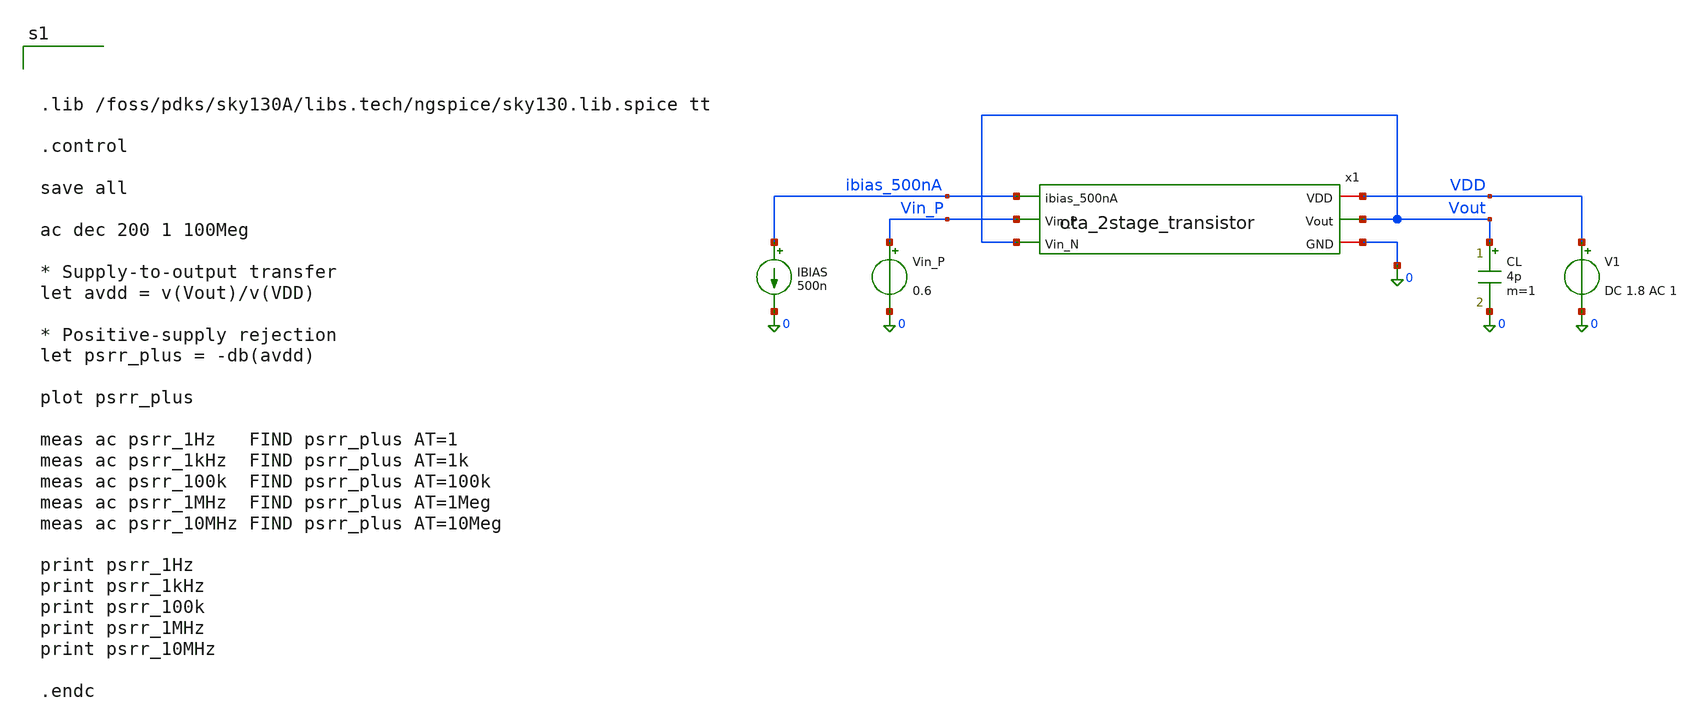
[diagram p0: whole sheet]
** sch_path: dfii/project_2stage_OTA_sim/tb_ota_2stage_psrr.sch
**.subckt tb_ota_2stage_psrr
x1 VDD ibias_500nA Vout Vin_P Vout 0 ota_2stage_transistor
V1 VDD 0 DC 1.8 AC 1
IBIAS ibias_500nA 0 500n
Vin_P Vin_P 0 0.6
CL Vout 0 4p m=1
**** begin user architecture code



.lib /foss/pdks/sky130A/libs.tech/ngspice/sky130.lib.spice tt

.control

save all

ac dec 200 1 100Meg

* Supply-to-output transfer
let avdd = v(Vout)/v(VDD)

* Positive-supply rejection
let psrr_plus = -db(avdd)

plot psrr_plus

meas ac psrr_1Hz   FIND psrr_plus AT=1
meas ac psrr_1kHz  FIND psrr_plus AT=1k
meas ac psrr_100k  FIND psrr_plus AT=100k
meas ac psrr_1MHz  FIND psrr_plus AT=1Meg
meas ac psrr_10MHz FIND psrr_plus AT=10Meg

print psrr_1Hz
print psrr_1kHz
print psrr_100k
print psrr_1MHz
print psrr_10MHz

.endc



**** end user architecture code
**.ends

* expanding   symbol:
*+  /foss/designs/project_2stage_OTA/dfii/project_2stage_OTA/ota_2stage_transistor.sym # of pins=6
** sym_path: dfii/project_2stage_OTA/ota_2stage_transistor.sym
** sch_path: dfii/project_2stage_OTA/ota_2stage_transistor.sch
.subckt ota_2stage_transistor VDD ibias_500nA Vout Vin_P Vin_N GND
*.iopin VDD
*.iopin GND
*.ipin ibias_500nA
*.ipin Vin_N
*.ipin Vin_P
*.opin Vout
XNLOAD_0 vdiode_n vdiode_n GND GND sky130_fd_pr__nfet_01v8 L=12 W=3.6 nf=1 ad='int((1 + 1)/2) * 3.6 / 1 * 0.29'
+ as='int((1 + 2)/2) * 3.6 / 1 * 0.29' pd='2*int((1 + 1)/2) * (3.6 / 1 + 0.29)' ps='2*int((1 + 2)/2) * (3.6 / 1 + 0.29)'
+ nrd='0.29 / 3.6 ' nrs='0.29 / 3.6 ' sa=0 sb=0 sd=0 mult=1 m=1
XNLOAD_1 out_s1 vdiode_n GND GND sky130_fd_pr__nfet_01v8 L=12 W=3.6 nf=1 ad='int((1 + 1)/2) * 3.6 / 1 * 0.29'
+ as='int((1 + 2)/2) * 3.6 / 1 * 0.29' pd='2*int((1 + 1)/2) * (3.6 / 1 + 0.29)' ps='2*int((1 + 2)/2) * (3.6 / 1 + 0.29)'
+ nrd='0.29 / 3.6 ' nrs='0.29 / 3.6 ' sa=0 sb=0 sd=0 mult=1 m=1
XNLOAD_2 Vout out_s1 GND GND sky130_fd_pr__nfet_01v8 L=2 W=3.6 nf=1 ad='int((1 + 1)/2) * 3.6 / 1 * 0.29'
+ as='int((1 + 2)/2) * 3.6 / 1 * 0.29' pd='2*int((1 + 1)/2) * (3.6 / 1 + 0.29)' ps='2*int((1 + 2)/2) * (3.6 / 1 + 0.29)'
+ nrd='0.29 / 3.6 ' nrs='0.29 / 3.6 ' sa=0 sb=0 sd=0 mult=2 m=2
XPDIFF_N vdiode_n Vin_N VCM VCM sky130_fd_pr__pfet_01v8 L=1 W=7.4 nf=1 ad='int((1 + 1)/2) * 7.4 / 1 * 0.29'
+ as='int((1 + 2)/2) * 7.4 / 1 * 0.29' pd='2*int((1 + 1)/2) * (7.4 / 1 + 0.29)' ps='2*int((1 + 2)/2) * (7.4 / 1 + 0.29)'
+ nrd='0.29 / 7.4 ' nrs='0.29 / 7.4 ' sa=0 sb=0 sd=0 mult=12 m=12
XPDIFF_P out_s1 Vin_P VCM VCM sky130_fd_pr__pfet_01v8 L=1 W=7.4 nf=1 ad='int((1 + 1)/2) * 7.4 / 1 * 0.29'
+ as='int((1 + 2)/2) * 7.4 / 1 * 0.29' pd='2*int((1 + 1)/2) * (7.4 / 1 + 0.29)' ps='2*int((1 + 2)/2) * (7.4 / 1 + 0.29)'
+ nrd='0.29 / 7.4 ' nrs='0.29 / 7.4 ' sa=0 sb=0 sd=0 mult=12 m=12
XPTAIL_1 VCM ibias_500nA VDD VDD sky130_fd_pr__pfet_01v8 L=1 W=1.76 nf=1 ad='int((1 + 1)/2) * 1.76 / 1 * 0.29'
+ as='int((1 + 2)/2) * 1.76 / 1 * 0.29' pd='2*int((1 + 1)/2) * (1.76 / 1 + 0.29)' ps='2*int((1 + 2)/2) * (1.76 / 1 + 0.29)'
+ nrd='0.29 / 1.76 ' nrs='0.29 / 1.76 ' sa=0 sb=0 sd=0 mult=1 m=1
XPTAIL_2 Vout ibias_500nA VDD VDD sky130_fd_pr__pfet_01v8 L=1 W=1.76 nf=1 ad='int((1 + 1)/2) * 1.76 / 1 * 0.29'
+ as='int((1 + 2)/2) * 1.76 / 1 * 0.29' pd='2*int((1 + 1)/2) * (1.76 / 1 + 0.29)' ps='2*int((1 + 2)/2) * (1.76 / 1 + 0.29)'
+ nrd='0.29 / 1.76 ' nrs='0.29 / 1.76 ' sa=0 sb=0 sd=0 mult=6 m=6
XPTAIL_0 ibias_500nA ibias_500nA VDD VDD sky130_fd_pr__pfet_01v8 L=1 W=1.76 nf=1 ad='int((1 + 1)/2) * 1.76 / 1 * 0.29'
+ as='int((1 + 2)/2) * 1.76 / 1 * 0.29' pd='2*int((1 + 1)/2) * (1.76 / 1 + 0.29)' ps='2*int((1 + 2)/2) * (1.76 / 1 + 0.29)'
+ nrd='0.29 / 1.76 ' nrs='0.29 / 1.76 ' sa=0 sb=0 sd=0 mult=1 m=1
XCMILLER out_s1 net1 sky130_fd_pr__cap_mim_m3_1 W=19 L=19 MF=1 m=1
XRMILLER Vout net1 GND sky130_fd_pr__res_xhigh_po_0p35 L=31.5 mult=1 m=1
.ends

.GLOBAL VDD
.end
